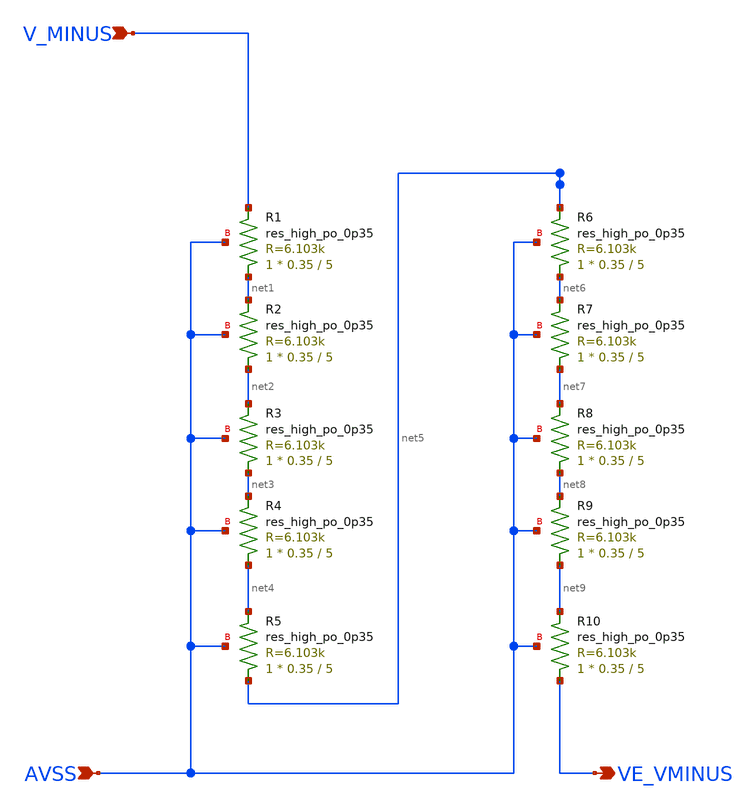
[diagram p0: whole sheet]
** sch_path: lef/bg2_res_array_vminus.sch
**.subckt bg2_res_array_vminus V_MINUS VE_VMINUS AVSS
*.ipin V_MINUS
*.opin VE_VMINUS
*.ipin AVSS
XR1 net1 V_MINUS AVSS sky130_fd_pr__res_high_po_0p35 L=5 mult=1 m=1
XR2 net2 net1 AVSS sky130_fd_pr__res_high_po_0p35 L=5 mult=1 m=1
XR3 net3 net2 AVSS sky130_fd_pr__res_high_po_0p35 L=5 mult=1 m=1
XR4 net4 net3 AVSS sky130_fd_pr__res_high_po_0p35 L=5 mult=1 m=1
XR5 net5 net4 AVSS sky130_fd_pr__res_high_po_0p35 L=5 mult=1 m=1
XR6 net6 net5 AVSS sky130_fd_pr__res_high_po_0p35 L=5 mult=1 m=1
XR7 net7 net6 AVSS sky130_fd_pr__res_high_po_0p35 L=5 mult=1 m=1
XR8 net8 net7 AVSS sky130_fd_pr__res_high_po_0p35 L=5 mult=1 m=1
XR9 net9 net8 AVSS sky130_fd_pr__res_high_po_0p35 L=5 mult=1 m=1
XR10 VE_VMINUS net9 AVSS sky130_fd_pr__res_high_po_0p35 L=5 mult=1 m=1
**.ends
.end
